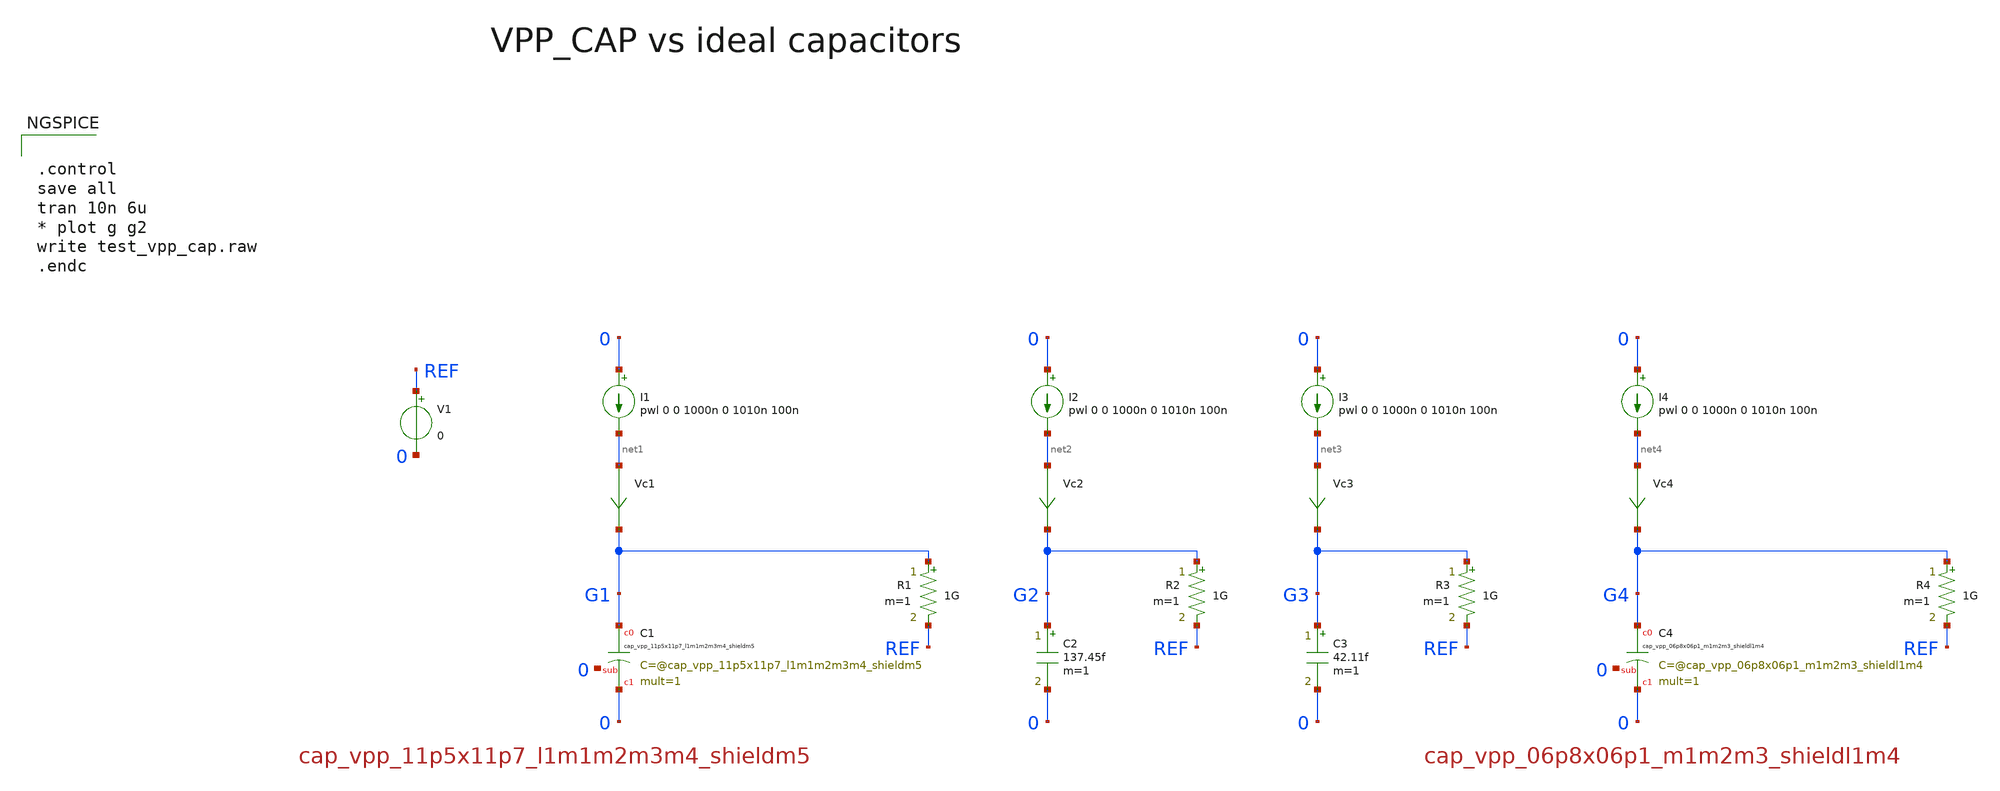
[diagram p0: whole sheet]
** sch_path: sky130A/xschem_libs/sky130_tests/test_vpp_cap/schematic/test_vpp_cap.sch
* Copyright 2021 Stefan Frederik Schippers
* Licensed under the Apache License, Version 2.0 (the "License");
* you may not use this file except in compliance with the License.
* You may obtain a copy of the License at
* https://www.apache.org/licenses/LICENSE-2.0
* Unless required by applicable law or agreed to in writing, software
* distributed under the License is distributed on an "AS IS" BASIS,
* WITHOUT WARRANTIES OR CONDITIONS OF ANY KIND, either express or implied.
* See the License for the specific language governing permissions and
* limitations under the License.
**.subckt test_vpp_cap
I1 0 net1 pwl 0 0 1000n 0 1010n 100n
R1 G1 REF 1G m=1
I3 0 net3 pwl 0 0 1000n 0 1010n 100n
R3 G3 REF 1G m=1
C2 G2 0 137.45f m=1
V1 REF 0 0
XC1 G1 0 0 sky130_fd_pr__cap_vpp_11p5x11p7_l1m1m2m3m4_shieldm5 mult=1 m=1
I2 0 net2 pwl 0 0 1000n 0 1010n 100n
R2 G2 REF 1G m=1
XC4 G4 0 0 sky130_fd_pr__cap_vpp_06p8x06p1_m1m2m3_shieldl1m4 mult=1 m=1
I4 0 net4 pwl 0 0 1000n 0 1010n 100n
R4 G4 REF 1G m=1
C3 G3 0 42.11f m=1
Vc1 net1 G1 0
.save i(vc1)
Vc2 net2 G2 0
.save i(vc2)
Vc3 net3 G3 0
.save i(vc3)
Vc4 net4 G4 0
.save i(vc4)
**** begin user architecture code


.control
save all
tran 10n 6u
* plot g g2
write test_vpp_cap.raw
.endc



** opencircuitdesign pdks install
.lib $::SKYWATER_MODELS/sky130.lib.spice tt

**** end user architecture code
**.ends
.end
